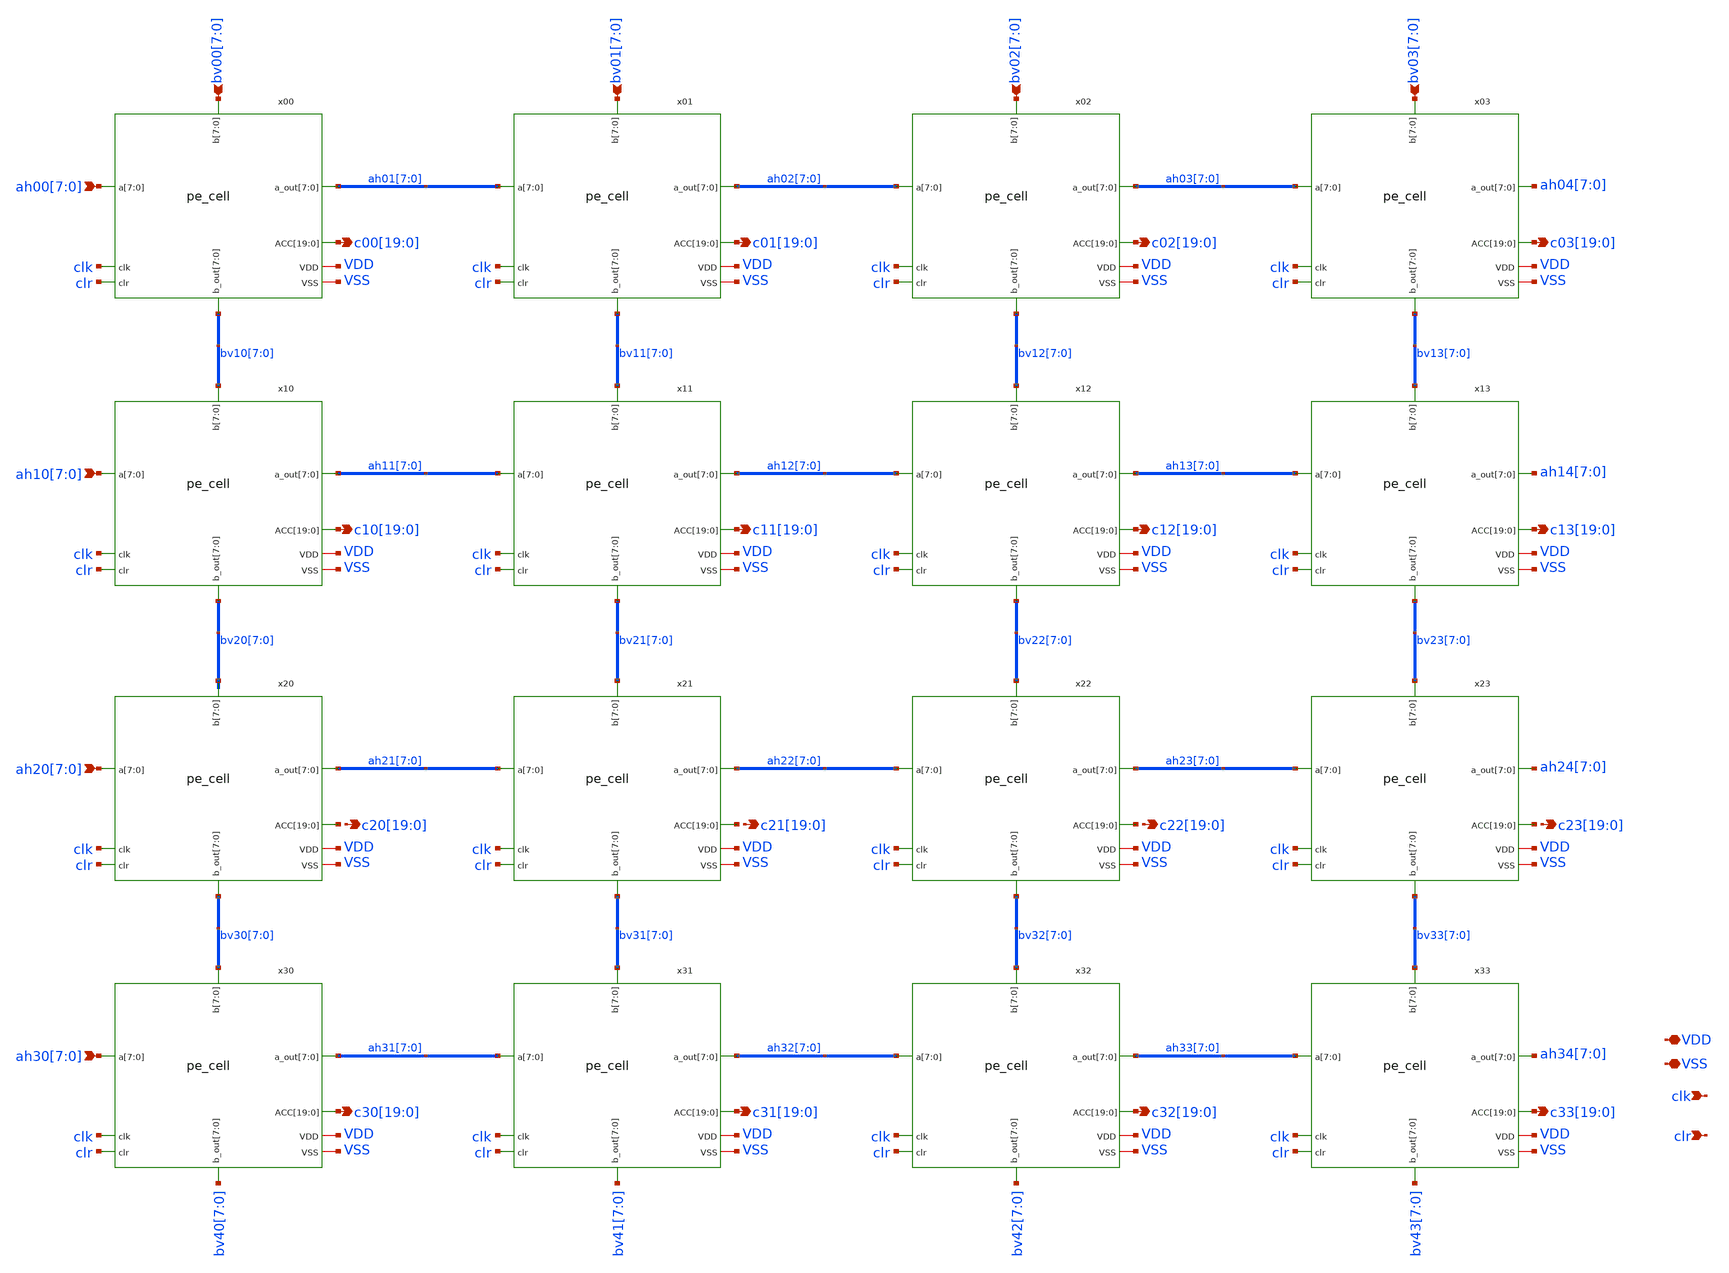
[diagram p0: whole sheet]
** sch_path: xschem/array4x4.sch
**.subckt array4x4 clk clr VSS VDD ah00[7],ah00[6],ah00[5],ah00[4],ah00[3],ah00[2],ah00[1],ah00[0]
*+ ah10[7],ah10[6],ah10[5],ah10[4],ah10[3],ah10[2],ah10[1],ah10[0] ah20[7],ah20[6],ah20[5],ah20[4],ah20[3],ah20[2],ah20[1],ah20[0]
*+ ah30[7],ah30[6],ah30[5],ah30[4],ah30[3],ah30[2],ah30[1],ah30[0] bv00[7],bv00[6],bv00[5],bv00[4],bv00[3],bv00[2],bv00[1],bv00[0]
*+ bv01[7],bv01[6],bv01[5],bv01[4],bv01[3],bv01[2],bv01[1],bv01[0] bv02[7],bv02[6],bv02[5],bv02[4],bv02[3],bv02[2],bv02[1],bv02[0]
*+ bv03[7],bv03[6],bv03[5],bv03[4],bv03[3],bv03[2],bv03[1],bv03[0]
*+ c00[19],c00[18],c00[17],c00[16],c00[15],c00[14],c00[13],c00[12],c00[11],c00[10],c00[9],c00[8],c00[7],c00[6],c00[5],c00[4],c00[3],c00[2],c00[1],c00[0]
*+ c01[19],c01[18],c01[17],c01[16],c01[15],c01[14],c01[13],c01[12],c01[11],c01[10],c01[9],c01[8],c01[7],c01[6],c01[5],c01[4],c01[3],c01[2],c01[1],c01[0]
*+ c02[19],c02[18],c02[17],c02[16],c02[15],c02[14],c02[13],c02[12],c02[11],c02[10],c02[9],c02[8],c02[7],c02[6],c02[5],c02[4],c02[3],c02[2],c02[1],c02[0]
*+ c03[19],c03[18],c03[17],c03[16],c03[15],c03[14],c03[13],c03[12],c03[11],c03[10],c03[9],c03[8],c03[7],c03[6],c03[5],c03[4],c03[3],c03[2],c03[1],c03[0]
*+ c10[19],c10[18],c10[17],c10[16],c10[15],c10[14],c10[13],c10[12],c10[11],c10[10],c10[9],c10[8],c10[7],c10[6],c10[5],c10[4],c10[3],c10[2],c10[1],c10[0]
*+ c11[19],c11[18],c11[17],c11[16],c11[15],c11[14],c11[13],c11[12],c11[11],c11[10],c11[9],c11[8],c11[7],c11[6],c11[5],c11[4],c11[3],c11[2],c11[1],c11[0]
*+ c12[19],c12[18],c12[17],c12[16],c12[15],c12[14],c12[13],c12[12],c12[11],c12[10],c12[9],c12[8],c12[7],c12[6],c12[5],c12[4],c12[3],c12[2],c12[1],c12[0]
*+ c13[19],c13[18],c13[17],c13[16],c13[15],c13[14],c13[13],c13[12],c13[11],c13[10],c13[9],c13[8],c13[7],c13[6],c13[5],c13[4],c13[3],c13[2],c13[1],c13[0]
*+ c20[19],c20[18],c20[17],c20[16],c20[15],c20[14],c20[13],c20[12],c20[11],c20[10],c20[9],c20[8],c20[7],c20[6],c20[5],c20[4],c20[3],c20[2],c20[1],c20[0]
*+ c21[19],c21[18],c21[17],c21[16],c21[15],c21[14],c21[13],c21[12],c21[11],c21[10],c21[9],c21[8],c21[7],c21[6],c21[5],c21[4],c21[3],c21[2],c21[1],c21[0]
*+ c22[19],c22[18],c22[17],c22[16],c22[15],c22[14],c22[13],c22[12],c22[11],c22[10],c22[9],c22[8],c22[7],c22[6],c22[5],c22[4],c22[3],c22[2],c22[1],c22[0]
*+ c23[19],c23[18],c23[17],c23[16],c23[15],c23[14],c23[13],c23[12],c23[11],c23[10],c23[9],c23[8],c23[7],c23[6],c23[5],c23[4],c23[3],c23[2],c23[1],c23[0]
*+ c30[19],c30[18],c30[17],c30[16],c30[15],c30[14],c30[13],c30[12],c30[11],c30[10],c30[9],c30[8],c30[7],c30[6],c30[5],c30[4],c30[3],c30[2],c30[1],c30[0]
*+ c31[19],c31[18],c31[17],c31[16],c31[15],c31[14],c31[13],c31[12],c31[11],c31[10],c31[9],c31[8],c31[7],c31[6],c31[5],c31[4],c31[3],c31[2],c31[1],c31[0]
*+ c32[19],c32[18],c32[17],c32[16],c32[15],c32[14],c32[13],c32[12],c32[11],c32[10],c32[9],c32[8],c32[7],c32[6],c32[5],c32[4],c32[3],c32[2],c32[1],c32[0]
*+ c33[19],c33[18],c33[17],c33[16],c33[15],c33[14],c33[13],c33[12],c33[11],c33[10],c33[9],c33[8],c33[7],c33[6],c33[5],c33[4],c33[3],c33[2],c33[1],c33[0]
*.ipin clk
*.ipin clr
*.iopin VSS
*.iopin VDD
*.ipin ah00[7],ah00[6],ah00[5],ah00[4],ah00[3],ah00[2],ah00[1],ah00[0]
*.ipin ah10[7],ah10[6],ah10[5],ah10[4],ah10[3],ah10[2],ah10[1],ah10[0]
*.ipin ah20[7],ah20[6],ah20[5],ah20[4],ah20[3],ah20[2],ah20[1],ah20[0]
*.ipin ah30[7],ah30[6],ah30[5],ah30[4],ah30[3],ah30[2],ah30[1],ah30[0]
*.ipin bv00[7],bv00[6],bv00[5],bv00[4],bv00[3],bv00[2],bv00[1],bv00[0]
*.ipin bv01[7],bv01[6],bv01[5],bv01[4],bv01[3],bv01[2],bv01[1],bv01[0]
*.ipin bv02[7],bv02[6],bv02[5],bv02[4],bv02[3],bv02[2],bv02[1],bv02[0]
*.ipin bv03[7],bv03[6],bv03[5],bv03[4],bv03[3],bv03[2],bv03[1],bv03[0]
*.opin
*+ c00[19],c00[18],c00[17],c00[16],c00[15],c00[14],c00[13],c00[12],c00[11],c00[10],c00[9],c00[8],c00[7],c00[6],c00[5],c00[4],c00[3],c00[2],c00[1],c00[0]
*.opin
*+ c01[19],c01[18],c01[17],c01[16],c01[15],c01[14],c01[13],c01[12],c01[11],c01[10],c01[9],c01[8],c01[7],c01[6],c01[5],c01[4],c01[3],c01[2],c01[1],c01[0]
*.opin
*+ c02[19],c02[18],c02[17],c02[16],c02[15],c02[14],c02[13],c02[12],c02[11],c02[10],c02[9],c02[8],c02[7],c02[6],c02[5],c02[4],c02[3],c02[2],c02[1],c02[0]
*.opin
*+ c03[19],c03[18],c03[17],c03[16],c03[15],c03[14],c03[13],c03[12],c03[11],c03[10],c03[9],c03[8],c03[7],c03[6],c03[5],c03[4],c03[3],c03[2],c03[1],c03[0]
*.opin
*+ c10[19],c10[18],c10[17],c10[16],c10[15],c10[14],c10[13],c10[12],c10[11],c10[10],c10[9],c10[8],c10[7],c10[6],c10[5],c10[4],c10[3],c10[2],c10[1],c10[0]
*.opin
*+ c11[19],c11[18],c11[17],c11[16],c11[15],c11[14],c11[13],c11[12],c11[11],c11[10],c11[9],c11[8],c11[7],c11[6],c11[5],c11[4],c11[3],c11[2],c11[1],c11[0]
*.opin
*+ c12[19],c12[18],c12[17],c12[16],c12[15],c12[14],c12[13],c12[12],c12[11],c12[10],c12[9],c12[8],c12[7],c12[6],c12[5],c12[4],c12[3],c12[2],c12[1],c12[0]
*.opin
*+ c13[19],c13[18],c13[17],c13[16],c13[15],c13[14],c13[13],c13[12],c13[11],c13[10],c13[9],c13[8],c13[7],c13[6],c13[5],c13[4],c13[3],c13[2],c13[1],c13[0]
*.opin
*+ c20[19],c20[18],c20[17],c20[16],c20[15],c20[14],c20[13],c20[12],c20[11],c20[10],c20[9],c20[8],c20[7],c20[6],c20[5],c20[4],c20[3],c20[2],c20[1],c20[0]
*.opin
*+ c21[19],c21[18],c21[17],c21[16],c21[15],c21[14],c21[13],c21[12],c21[11],c21[10],c21[9],c21[8],c21[7],c21[6],c21[5],c21[4],c21[3],c21[2],c21[1],c21[0]
*.opin
*+ c22[19],c22[18],c22[17],c22[16],c22[15],c22[14],c22[13],c22[12],c22[11],c22[10],c22[9],c22[8],c22[7],c22[6],c22[5],c22[4],c22[3],c22[2],c22[1],c22[0]
*.opin
*+ c23[19],c23[18],c23[17],c23[16],c23[15],c23[14],c23[13],c23[12],c23[11],c23[10],c23[9],c23[8],c23[7],c23[6],c23[5],c23[4],c23[3],c23[2],c23[1],c23[0]
*.opin
*+ c30[19],c30[18],c30[17],c30[16],c30[15],c30[14],c30[13],c30[12],c30[11],c30[10],c30[9],c30[8],c30[7],c30[6],c30[5],c30[4],c30[3],c30[2],c30[1],c30[0]
*.opin
*+ c31[19],c31[18],c31[17],c31[16],c31[15],c31[14],c31[13],c31[12],c31[11],c31[10],c31[9],c31[8],c31[7],c31[6],c31[5],c31[4],c31[3],c31[2],c31[1],c31[0]
*.opin
*+ c32[19],c32[18],c32[17],c32[16],c32[15],c32[14],c32[13],c32[12],c32[11],c32[10],c32[9],c32[8],c32[7],c32[6],c32[5],c32[4],c32[3],c32[2],c32[1],c32[0]
*.opin
*+ c33[19],c33[18],c33[17],c33[16],c33[15],c33[14],c33[13],c33[12],c33[11],c33[10],c33[9],c33[8],c33[7],c33[6],c33[5],c33[4],c33[3],c33[2],c33[1],c33[0]
x00 bv10[7] bv10[6] bv10[5] bv10[4] bv10[3] bv10[2] bv10[1] bv10[0] ah00[7] ah00[6] ah00[5] ah00[4]
+ ah00[3] ah00[2] ah00[1] ah00[0] bv00[7] bv00[6] bv00[5] bv00[4] bv00[3] bv00[2] bv00[1] bv00[0] c00[19]
+ c00[18] c00[17] c00[16] c00[15] c00[14] c00[13] c00[12] c00[11] c00[10] c00[9] c00[8] c00[7] c00[6] c00[5]
+ c00[4] c00[3] c00[2] c00[1] c00[0] VDD clk VSS clr ah01[7] ah01[6] ah01[5] ah01[4] ah01[3] ah01[2] ah01[1]
+ ah01[0] pe_cell
x01 bv11[7] bv11[6] bv11[5] bv11[4] bv11[3] bv11[2] bv11[1] bv11[0] ah01[7] ah01[6] ah01[5] ah01[4]
+ ah01[3] ah01[2] ah01[1] ah01[0] bv01[7] bv01[6] bv01[5] bv01[4] bv01[3] bv01[2] bv01[1] bv01[0] c01[19]
+ c01[18] c01[17] c01[16] c01[15] c01[14] c01[13] c01[12] c01[11] c01[10] c01[9] c01[8] c01[7] c01[6] c01[5]
+ c01[4] c01[3] c01[2] c01[1] c01[0] VDD clk VSS clr ah02[7] ah02[6] ah02[5] ah02[4] ah02[3] ah02[2] ah02[1]
+ ah02[0] pe_cell
x02 bv12[7] bv12[6] bv12[5] bv12[4] bv12[3] bv12[2] bv12[1] bv12[0] ah02[7] ah02[6] ah02[5] ah02[4]
+ ah02[3] ah02[2] ah02[1] ah02[0] bv02[7] bv02[6] bv02[5] bv02[4] bv02[3] bv02[2] bv02[1] bv02[0] c02[19]
+ c02[18] c02[17] c02[16] c02[15] c02[14] c02[13] c02[12] c02[11] c02[10] c02[9] c02[8] c02[7] c02[6] c02[5]
+ c02[4] c02[3] c02[2] c02[1] c02[0] VDD clk VSS clr ah03[7] ah03[6] ah03[5] ah03[4] ah03[3] ah03[2] ah03[1]
+ ah03[0] pe_cell
x03 bv13[7] bv13[6] bv13[5] bv13[4] bv13[3] bv13[2] bv13[1] bv13[0] ah03[7] ah03[6] ah03[5] ah03[4]
+ ah03[3] ah03[2] ah03[1] ah03[0] bv03[7] bv03[6] bv03[5] bv03[4] bv03[3] bv03[2] bv03[1] bv03[0] c03[19]
+ c03[18] c03[17] c03[16] c03[15] c03[14] c03[13] c03[12] c03[11] c03[10] c03[9] c03[8] c03[7] c03[6] c03[5]
+ c03[4] c03[3] c03[2] c03[1] c03[0] VDD clk VSS clr ah04[7] ah04[6] ah04[5] ah04[4] ah04[3] ah04[2] ah04[1]
+ ah04[0] pe_cell
x10 bv20[7] bv20[6] bv20[5] bv20[4] bv20[3] bv20[2] bv20[1] bv20[0] ah10[7] ah10[6] ah10[5] ah10[4]
+ ah10[3] ah10[2] ah10[1] ah10[0] bv10[7] bv10[6] bv10[5] bv10[4] bv10[3] bv10[2] bv10[1] bv10[0] c10[19]
+ c10[18] c10[17] c10[16] c10[15] c10[14] c10[13] c10[12] c10[11] c10[10] c10[9] c10[8] c10[7] c10[6] c10[5]
+ c10[4] c10[3] c10[2] c10[1] c10[0] VDD clk VSS clr ah11[7] ah11[6] ah11[5] ah11[4] ah11[3] ah11[2] ah11[1]
+ ah11[0] pe_cell
x11 bv21[7] bv21[6] bv21[5] bv21[4] bv21[3] bv21[2] bv21[1] bv21[0] ah11[7] ah11[6] ah11[5] ah11[4]
+ ah11[3] ah11[2] ah11[1] ah11[0] bv11[7] bv11[6] bv11[5] bv11[4] bv11[3] bv11[2] bv11[1] bv11[0] c11[19]
+ c11[18] c11[17] c11[16] c11[15] c11[14] c11[13] c11[12] c11[11] c11[10] c11[9] c11[8] c11[7] c11[6] c11[5]
+ c11[4] c11[3] c11[2] c11[1] c11[0] VDD clk VSS clr ah12[7] ah12[6] ah12[5] ah12[4] ah12[3] ah12[2] ah12[1]
+ ah12[0] pe_cell
x12 bv22[7] bv22[6] bv22[5] bv22[4] bv22[3] bv22[2] bv22[1] bv22[0] ah12[7] ah12[6] ah12[5] ah12[4]
+ ah12[3] ah12[2] ah12[1] ah12[0] bv12[7] bv12[6] bv12[5] bv12[4] bv12[3] bv12[2] bv12[1] bv12[0] c12[19]
+ c12[18] c12[17] c12[16] c12[15] c12[14] c12[13] c12[12] c12[11] c12[10] c12[9] c12[8] c12[7] c12[6] c12[5]
+ c12[4] c12[3] c12[2] c12[1] c12[0] VDD clk VSS clr ah13[7] ah13[6] ah13[5] ah13[4] ah13[3] ah13[2] ah13[1]
+ ah13[0] pe_cell
x13 bv23[7] bv23[6] bv23[5] bv23[4] bv23[3] bv23[2] bv23[1] bv23[0] ah13[7] ah13[6] ah13[5] ah13[4]
+ ah13[3] ah13[2] ah13[1] ah13[0] bv13[7] bv13[6] bv13[5] bv13[4] bv13[3] bv13[2] bv13[1] bv13[0] c13[19]
+ c13[18] c13[17] c13[16] c13[15] c13[14] c13[13] c13[12] c13[11] c13[10] c13[9] c13[8] c13[7] c13[6] c13[5]
+ c13[4] c13[3] c13[2] c13[1] c13[0] VDD clk VSS clr ah14[7] ah14[6] ah14[5] ah14[4] ah14[3] ah14[2] ah14[1]
+ ah14[0] pe_cell
x20 bv30[7] bv30[6] bv30[5] bv30[4] bv30[3] bv30[2] bv30[1] bv30[0] ah20[7] ah20[6] ah20[5] ah20[4]
+ ah20[3] ah20[2] ah20[1] ah20[0] bv20[7] bv20[6] bv20[5] bv20[4] bv20[3] bv20[2] bv20[1] bv20[0] net1[19]
+ net1[18] net1[17] net1[16] net1[15] net1[14] net1[13] net1[12] net1[11] net1[10] net1[9] net1[8] net1[7]
+ net1[6] net1[5] net1[4] net1[3] net1[2] net1[1] net1[0] VDD clk VSS clr ah21[7] ah21[6] ah21[5] ah21[4]
+ ah21[3] ah21[2] ah21[1] ah21[0] pe_cell
x21 bv31[7] bv31[6] bv31[5] bv31[4] bv31[3] bv31[2] bv31[1] bv31[0] ah21[7] ah21[6] ah21[5] ah21[4]
+ ah21[3] ah21[2] ah21[1] ah21[0] bv21[7] bv21[6] bv21[5] bv21[4] bv21[3] bv21[2] bv21[1] bv21[0] net2[19]
+ net2[18] net2[17] net2[16] net2[15] net2[14] net2[13] net2[12] net2[11] net2[10] net2[9] net2[8] net2[7]
+ net2[6] net2[5] net2[4] net2[3] net2[2] net2[1] net2[0] VDD clk VSS clr ah22[7] ah22[6] ah22[5] ah22[4]
+ ah22[3] ah22[2] ah22[1] ah22[0] pe_cell
x22 bv32[7] bv32[6] bv32[5] bv32[4] bv32[3] bv32[2] bv32[1] bv32[0] ah22[7] ah22[6] ah22[5] ah22[4]
+ ah22[3] ah22[2] ah22[1] ah22[0] bv22[7] bv22[6] bv22[5] bv22[4] bv22[3] bv22[2] bv22[1] bv22[0] net3[19]
+ net3[18] net3[17] net3[16] net3[15] net3[14] net3[13] net3[12] net3[11] net3[10] net3[9] net3[8] net3[7]
+ net3[6] net3[5] net3[4] net3[3] net3[2] net3[1] net3[0] VDD clk VSS clr ah23[7] ah23[6] ah23[5] ah23[4]
+ ah23[3] ah23[2] ah23[1] ah23[0] pe_cell
x23 bv33[7] bv33[6] bv33[5] bv33[4] bv33[3] bv33[2] bv33[1] bv33[0] ah23[7] ah23[6] ah23[5] ah23[4]
+ ah23[3] ah23[2] ah23[1] ah23[0] bv23[7] bv23[6] bv23[5] bv23[4] bv23[3] bv23[2] bv23[1] bv23[0] net4[19]
+ net4[18] net4[17] net4[16] net4[15] net4[14] net4[13] net4[12] net4[11] net4[10] net4[9] net4[8] net4[7]
+ net4[6] net4[5] net4[4] net4[3] net4[2] net4[1] net4[0] VDD clk VSS clr ah24[7] ah24[6] ah24[5] ah24[4]
+ ah24[3] ah24[2] ah24[1] ah24[0] pe_cell
x30 bv40[7] bv40[6] bv40[5] bv40[4] bv40[3] bv40[2] bv40[1] bv40[0] ah30[7] ah30[6] ah30[5] ah30[4]
+ ah30[3] ah30[2] ah30[1] ah30[0] bv30[7] bv30[6] bv30[5] bv30[4] bv30[3] bv30[2] bv30[1] bv30[0] c30[19]
+ c30[18] c30[17] c30[16] c30[15] c30[14] c30[13] c30[12] c30[11] c30[10] c30[9] c30[8] c30[7] c30[6] c30[5]
+ c30[4] c30[3] c30[2] c30[1] c30[0] VDD clk VSS clr ah31[7] ah31[6] ah31[5] ah31[4] ah31[3] ah31[2] ah31[1]
+ ah31[0] pe_cell
x31 bv41[7] bv41[6] bv41[5] bv41[4] bv41[3] bv41[2] bv41[1] bv41[0] ah31[7] ah31[6] ah31[5] ah31[4]
+ ah31[3] ah31[2] ah31[1] ah31[0] bv31[7] bv31[6] bv31[5] bv31[4] bv31[3] bv31[2] bv31[1] bv31[0] c31[19]
+ c31[18] c31[17] c31[16] c31[15] c31[14] c31[13] c31[12] c31[11] c31[10] c31[9] c31[8] c31[7] c31[6] c31[5]
+ c31[4] c31[3] c31[2] c31[1] c31[0] VDD clk VSS clr ah32[7] ah32[6] ah32[5] ah32[4] ah32[3] ah32[2] ah32[1]
+ ah32[0] pe_cell
x32 bv42[7] bv42[6] bv42[5] bv42[4] bv42[3] bv42[2] bv42[1] bv42[0] ah32[7] ah32[6] ah32[5] ah32[4]
+ ah32[3] ah32[2] ah32[1] ah32[0] bv32[7] bv32[6] bv32[5] bv32[4] bv32[3] bv32[2] bv32[1] bv32[0] c32[19]
+ c32[18] c32[17] c32[16] c32[15] c32[14] c32[13] c32[12] c32[11] c32[10] c32[9] c32[8] c32[7] c32[6] c32[5]
+ c32[4] c32[3] c32[2] c32[1] c32[0] VDD clk VSS clr ah33[7] ah33[6] ah33[5] ah33[4] ah33[3] ah33[2] ah33[1]
+ ah33[0] pe_cell
x33 bv43[7] bv43[6] bv43[5] bv43[4] bv43[3] bv43[2] bv43[1] bv43[0] ah33[7] ah33[6] ah33[5] ah33[4]
+ ah33[3] ah33[2] ah33[1] ah33[0] bv33[7] bv33[6] bv33[5] bv33[4] bv33[3] bv33[2] bv33[1] bv33[0] c33[19]
+ c33[18] c33[17] c33[16] c33[15] c33[14] c33[13] c33[12] c33[11] c33[10] c33[9] c33[8] c33[7] c33[6] c33[5]
+ c33[4] c33[3] c33[2] c33[1] c33[0] VDD clk VSS clr ah34[7] ah34[6] ah34[5] ah34[4] ah34[3] ah34[2] ah34[1]
+ ah34[0] pe_cell
**.ends
.end
